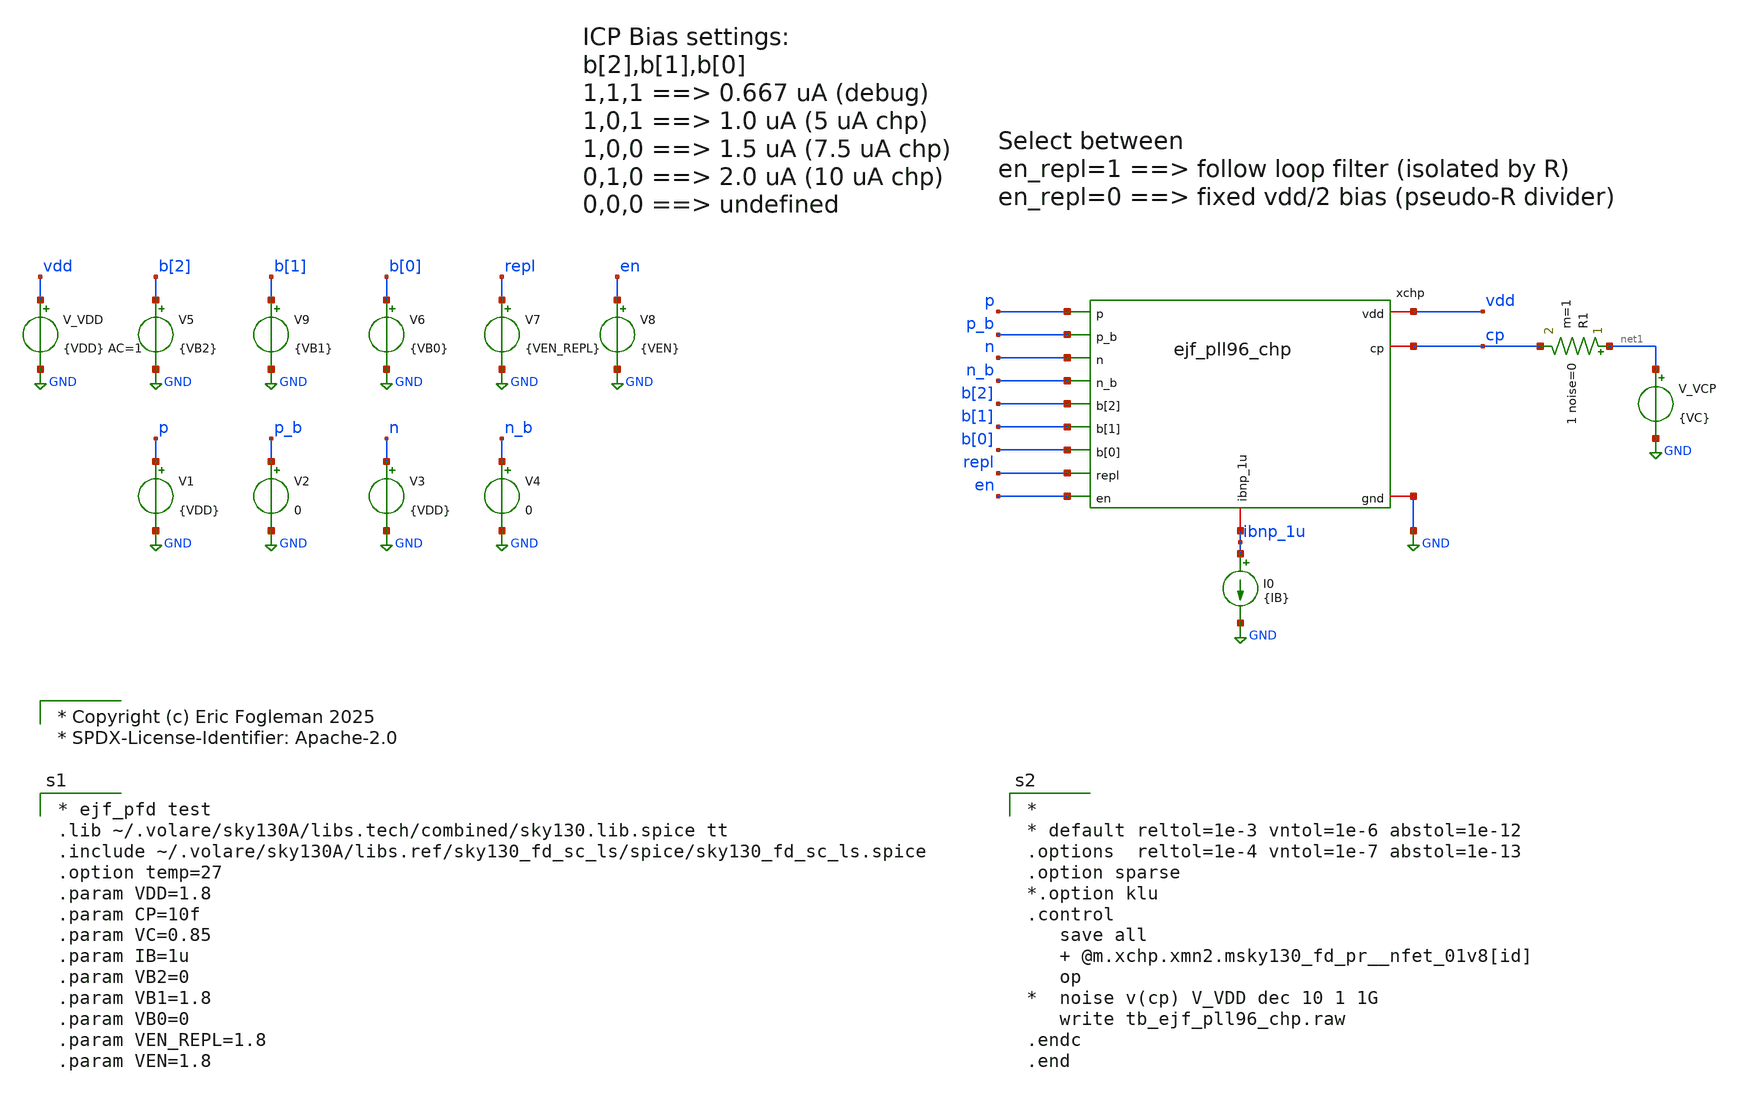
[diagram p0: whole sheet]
** sch_path: xschem/tb_ejf_pll96_chp.sch

* Copyright (c) Eric Fogleman 2025
* SPDX-License-Identifier: Apache-2.0

**.subckt tb_ejf_pll96_chp
V_VDD vdd GND {VDD} AC=1
.save i(v_vdd)
xchp vdd p ibnp_1u p_b cp n_b n GND b[1] repl en b[2] b[0] ejf_pll96_chp
I0 ibnp_1u GND {IB}
V_VCP net1 GND {VC}
.save i(v_vcp)
V1 p GND {VDD}
.save i(v1)
V2 p_b GND 0
.save i(v2)
V3 n GND {VDD}
.save i(v3)
V4 n_b GND 0
.save i(v4)
R1 net1 cp 1 noise=0 m=1
V5 b[2] GND {VB2}
.save i(v5)
V6 b[0] GND {VB0}
.save i(v6)
V7 repl GND {VEN_REPL}
.save i(v7)
V8 en GND {VEN}
.save i(v8)
V9 b[1] GND {VB1}
.save i(v9)
**** begin user architecture code

* ejf_pfd test
.lib ~/.volare/sky130A/libs.tech/combined/sky130.lib.spice tt
.include ~/.volare/sky130A/libs.ref/sky130_fd_sc_ls/spice/sky130_fd_sc_ls.spice
.option temp=27
.param VDD=1.8
.param CP=10f
.param VC=0.85
.param IB=1u
.param VB2=0
.param VB1=1.8
.param VB0=0
.param VEN_REPL=1.8
.param VEN=1.8



*
* default reltol=1e-3 vntol=1e-6 abstol=1e-12
.options  reltol=1e-4 vntol=1e-7 abstol=1e-13
.option sparse
*.option klu
.control
   save all
   + @m.xchp.xmn2.msky130_fd_pr__nfet_01v8[id]
   op
*  noise v(cp) V_VDD dec 10 1 1G
   write tb_ejf_pll96_chp.raw
.endc
.end

**** end user architecture code
**.ends
.GLOBAL GND
.end
